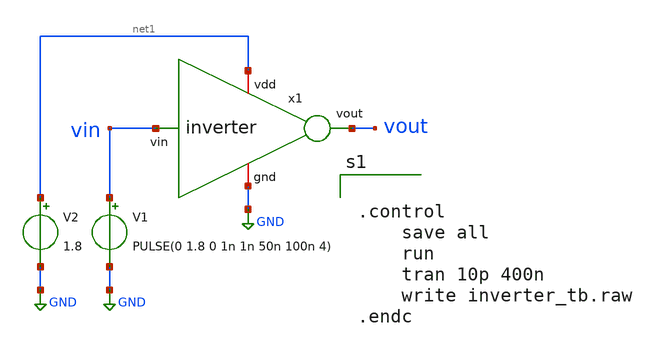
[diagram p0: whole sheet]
** sch_path: inverter/inverter_tb.sch
**.subckt inverter_tb
x1 net1 vout vin GND inverter
V1 vin GND PULSE(0 1.8 0 1n 1n 50n 100n 4)
.save i(v1)
V2 net1 GND 1.8
.save i(v2)
**** begin user architecture code


.control
	save all
	run
	tran 10p 400n
	write inverter_tb.raw
.endc



** opencircuitdesign pdks install
.lib $::SKYWATER_MODELS/sky130.lib.spice tt


**** end user architecture code
**.ends
.GLOBAL GND
.end
